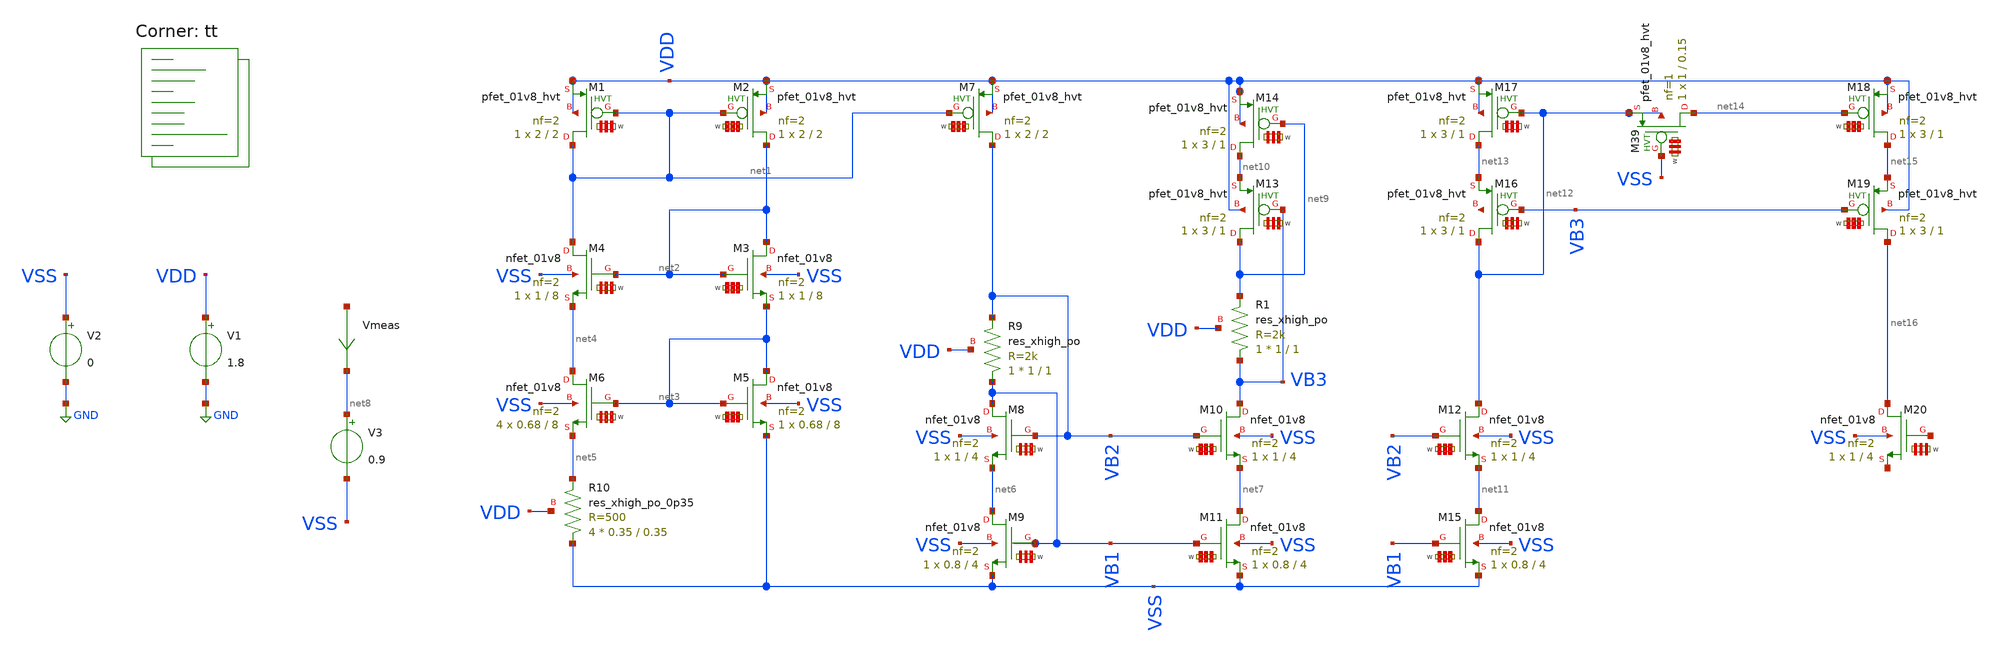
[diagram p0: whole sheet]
** sch_path: my_ip/sky130A/VFCOA_v1/testbench.sch
**.subckt testbench
V1 VDD GND 1.8
V2 VSS GND 0
V3 net8 VSS 0.9
XM5 net3 net3 VSS VSS sky130_fd_pr__nfet_01v8 L=8 W='0.68 * 2 ' nf=2 ad='int((2 + 1)/2) * 0.68 / 2 * 0.29'
+ as='int((2 + 2)/2) * 0.68 / 2 * 0.29' pd='2*int((2 + 1)/2) * (0.68 / 2 + 0.29)' ps='2*int((2 + 2)/2) * (0.68 / 2 + 0.29)'
+ nrd='0.29 / 0.68 ' nrs='0.29 / 0.68 ' sa=0 sb=0 sd=0 mult=1 m=1
XM6 net4 net3 net5 VSS sky130_fd_pr__nfet_01v8 L=8 W='0.68 * 2 ' nf=2 ad='int((2 + 1)/2) * 0.68 / 2 * 0.29'
+ as='int((2 + 2)/2) * 0.68 / 2 * 0.29' pd='2*int((2 + 1)/2) * (0.68 / 2 + 0.29)' ps='2*int((2 + 2)/2) * (0.68 / 2 + 0.29)'
+ nrd='0.29 / 0.68 ' nrs='0.29 / 0.68 ' sa=0 sb=0 sd=0 mult=4 m=4
XM2 net2 net1 VDD VDD sky130_fd_pr__pfet_01v8_hvt L=2 W='2 * 2 ' nf=2 ad='int((2 + 1)/2) * 2 / 2 * 0.29'
+ as='int((2 + 2)/2) * 2 / 2 * 0.29' pd='2*int((2 + 1)/2) * (2 / 2 + 0.29)' ps='2*int((2 + 2)/2) * (2 / 2 + 0.29)'
+ nrd='0.29 / 2 ' nrs='0.29 / 2 ' sa=0 sb=0 sd=0 mult=1 m=1
XM1 net1 net1 VDD VDD sky130_fd_pr__pfet_01v8_hvt L=2 W='2 * 2 ' nf=2 ad='int((2 + 1)/2) * 2 / 2 * 0.29'
+ as='int((2 + 2)/2) * 2 / 2 * 0.29' pd='2*int((2 + 1)/2) * (2 / 2 + 0.29)' ps='2*int((2 + 2)/2) * (2 / 2 + 0.29)'
+ nrd='0.29 / 2 ' nrs='0.29 / 2 ' sa=0 sb=0 sd=0 mult=1 m=1
XR10 VSS net5 VDD sky130_fd_pr__res_xhigh_po_0p35 L=0.35 mult=4 m=4
XM4 net1 net2 net4 VSS sky130_fd_pr__nfet_01v8 L=8 W='1 * 2 ' nf=2 ad='int((2 + 1)/2) * 1 / 2 * 0.29'
+ as='int((2 + 2)/2) * 1 / 2 * 0.29' pd='2*int((2 + 1)/2) * (1 / 2 + 0.29)' ps='2*int((2 + 2)/2) * (1 / 2 + 0.29)'
+ nrd='0.29 / 1 ' nrs='0.29 / 1 ' sa=0 sb=0 sd=0 mult=1 m=1
XM3 net2 net2 net3 VSS sky130_fd_pr__nfet_01v8 L=8 W='1 * 2 ' nf=2 ad='int((2 + 1)/2) * 1 / 2 * 0.29'
+ as='int((2 + 2)/2) * 1 / 2 * 0.29' pd='2*int((2 + 1)/2) * (1 / 2 + 0.29)' ps='2*int((2 + 2)/2) * (1 / 2 + 0.29)'
+ nrd='0.29 / 1 ' nrs='0.29 / 1 ' sa=0 sb=0 sd=0 mult=1 m=1
XM7 VB2 net1 VDD VDD sky130_fd_pr__pfet_01v8_hvt L=2 W='2 * 2 ' nf=2 ad='int((2 + 1)/2) * 2 / 2 * 0.29'
+ as='int((2 + 2)/2) * 2 / 2 * 0.29' pd='2*int((2 + 1)/2) * (2 / 2 + 0.29)' ps='2*int((2 + 2)/2) * (2 / 2 + 0.29)'
+ nrd='0.29 / 2 ' nrs='0.29 / 2 ' sa=0 sb=0 sd=0 mult=1 m=1
Vmeas net17 net8 0
.save i(vmeas)
XM10 VB3 VB2 net7 VSS sky130_fd_pr__nfet_01v8 L=4 W='1 * 2 ' nf=2 ad='int((2 + 1)/2) * 1 / 2 * 0.29'
+ as='int((2 + 2)/2) * 1 / 2 * 0.29' pd='2*int((2 + 1)/2) * (1 / 2 + 0.29)' ps='2*int((2 + 2)/2) * (1 / 2 + 0.29)'
+ nrd='0.29 / 1 ' nrs='0.29 / 1 ' sa=0 sb=0 sd=0 mult=1 m=1
XR9 VB1 VB2 VDD sky130_fd_pr__res_xhigh_po W=1 L=1 mult=1 m=1
XM11 net7 VB1 VSS VSS sky130_fd_pr__nfet_01v8 L=4 W='0.8 * 2 ' nf=2 ad='int((2 + 1)/2) * 0.8 / 2 * 0.29'
+ as='int((2 + 2)/2) * 0.8 / 2 * 0.29' pd='2*int((2 + 1)/2) * (0.8 / 2 + 0.29)' ps='2*int((2 + 2)/2) * (0.8 / 2 + 0.29)'
+ nrd='0.29 / 0.8 ' nrs='0.29 / 0.8 ' sa=0 sb=0 sd=0 mult=1 m=1
XM8 VB1 VB2 net6 VSS sky130_fd_pr__nfet_01v8 L=4 W='1 * 2 ' nf=2 ad='int((2 + 1)/2) * 1 / 2 * 0.29' as='int((2 + 2)/2) * 1 / 2 * 0.29'
+ pd='2*int((2 + 1)/2) * (1 / 2 + 0.29)' ps='2*int((2 + 2)/2) * (1 / 2 + 0.29)' nrd='0.29 / 1 ' nrs='0.29 / 1 '
+ sa=0 sb=0 sd=0 mult=1 m=1
XM9 net6 VB1 VSS VSS sky130_fd_pr__nfet_01v8 L=4 W='0.8 * 2 ' nf=2 ad='int((2 + 1)/2) * 0.8 / 2 * 0.29'
+ as='int((2 + 2)/2) * 0.8 / 2 * 0.29' pd='2*int((2 + 1)/2) * (0.8 / 2 + 0.29)' ps='2*int((2 + 2)/2) * (0.8 / 2 + 0.29)'
+ nrd='0.29 / 0.8 ' nrs='0.29 / 0.8 ' sa=0 sb=0 sd=0 mult=1 m=1
XR1 VB3 net9 VDD sky130_fd_pr__res_xhigh_po W=1 L=1 mult=1 m=1
XM13 net9 VB3 net10 VDD sky130_fd_pr__pfet_01v8_hvt L=1 W='3 * 2 ' nf=2 ad='int((2 + 1)/2) * 3 / 2 * 0.29'
+ as='int((2 + 2)/2) * 3 / 2 * 0.29' pd='2*int((2 + 1)/2) * (3 / 2 + 0.29)' ps='2*int((2 + 2)/2) * (3 / 2 + 0.29)'
+ nrd='0.29 / 3 ' nrs='0.29 / 3 ' sa=0 sb=0 sd=0 mult=1 m=1
XM14 net10 net9 VDD VDD sky130_fd_pr__pfet_01v8_hvt L=1 W='3 * 2 ' nf=2 ad='int((2 + 1)/2) * 3 / 2 * 0.29'
+ as='int((2 + 2)/2) * 3 / 2 * 0.29' pd='2*int((2 + 1)/2) * (3 / 2 + 0.29)' ps='2*int((2 + 2)/2) * (3 / 2 + 0.29)'
+ nrd='0.29 / 3 ' nrs='0.29 / 3 ' sa=0 sb=0 sd=0 mult=1 m=1
XM12 net12 VB2 net11 VSS sky130_fd_pr__nfet_01v8 L=4 W='1 * 2 ' nf=2 ad='int((2 + 1)/2) * 1 / 2 * 0.29'
+ as='int((2 + 2)/2) * 1 / 2 * 0.29' pd='2*int((2 + 1)/2) * (1 / 2 + 0.29)' ps='2*int((2 + 2)/2) * (1 / 2 + 0.29)'
+ nrd='0.29 / 1 ' nrs='0.29 / 1 ' sa=0 sb=0 sd=0 mult=1 m=1
XM15 net11 VB1 VSS VSS sky130_fd_pr__nfet_01v8 L=4 W='0.8 * 2 ' nf=2 ad='int((2 + 1)/2) * 0.8 / 2 * 0.29'
+ as='int((2 + 2)/2) * 0.8 / 2 * 0.29' pd='2*int((2 + 1)/2) * (0.8 / 2 + 0.29)' ps='2*int((2 + 2)/2) * (0.8 / 2 + 0.29)'
+ nrd='0.29 / 0.8 ' nrs='0.29 / 0.8 ' sa=0 sb=0 sd=0 mult=1 m=1
XM16 net12 VB3 net13 net18 sky130_fd_pr__pfet_01v8_hvt L=1 W='3 * 2 ' nf=2 ad='int((2 + 1)/2) * 3 / 2 * 0.29'
+ as='int((2 + 2)/2) * 3 / 2 * 0.29' pd='2*int((2 + 1)/2) * (3 / 2 + 0.29)' ps='2*int((2 + 2)/2) * (3 / 2 + 0.29)'
+ nrd='0.29 / 3 ' nrs='0.29 / 3 ' sa=0 sb=0 sd=0 mult=1 m=1
XM17 net13 net12 VDD VDD sky130_fd_pr__pfet_01v8_hvt L=1 W='3 * 2 ' nf=2 ad='int((2 + 1)/2) * 3 / 2 * 0.29'
+ as='int((2 + 2)/2) * 3 / 2 * 0.29' pd='2*int((2 + 1)/2) * (3 / 2 + 0.29)' ps='2*int((2 + 2)/2) * (3 / 2 + 0.29)'
+ nrd='0.29 / 3 ' nrs='0.29 / 3 ' sa=0 sb=0 sd=0 mult=1 m=1
XM39 net14 VSS net12 net12 sky130_fd_pr__pfet_01v8_hvt L=0.15 W='1 * 1 ' nf=1 ad='int((1 + 1)/2) * 1 / 1 * 0.29'
+ as='int((1 + 2)/2) * 1 / 1 * 0.29' pd='2*int((1 + 1)/2) * (1 / 1 + 0.29)' ps='2*int((1 + 2)/2) * (1 / 1 + 0.29)'
+ nrd='0.29 / 1 ' nrs='0.29 / 1 ' sa=0 sb=0 sd=0 mult=1 m=1
XM18 net15 net14 VDD VDD sky130_fd_pr__pfet_01v8_hvt L=1 W='3 * 2 ' nf=2 ad='int((2 + 1)/2) * 3 / 2 * 0.29'
+ as='int((2 + 2)/2) * 3 / 2 * 0.29' pd='2*int((2 + 1)/2) * (3 / 2 + 0.29)' ps='2*int((2 + 2)/2) * (3 / 2 + 0.29)'
+ nrd='0.29 / 3 ' nrs='0.29 / 3 ' sa=0 sb=0 sd=0 mult=1 m=1
XM19 net16 VB3 net15 VDD sky130_fd_pr__pfet_01v8_hvt L=1 W='3 * 2 ' nf=2 ad='int((2 + 1)/2) * 3 / 2 * 0.29'
+ as='int((2 + 2)/2) * 3 / 2 * 0.29' pd='2*int((2 + 1)/2) * (3 / 2 + 0.29)' ps='2*int((2 + 2)/2) * (3 / 2 + 0.29)'
+ nrd='0.29 / 3 ' nrs='0.29 / 3 ' sa=0 sb=0 sd=0 mult=1 m=1
XM20 net16 net19 net20 VSS sky130_fd_pr__nfet_01v8 L=4 W='1 * 2 ' nf=2 ad='int((2 + 1)/2) * 1 / 2 * 0.29'
+ as='int((2 + 2)/2) * 1 / 2 * 0.29' pd='2*int((2 + 1)/2) * (1 / 2 + 0.29)' ps='2*int((2 + 2)/2) * (1 / 2 + 0.29)'
+ nrd='0.29 / 1 ' nrs='0.29 / 1 ' sa=0 sb=0 sd=0 mult=1 m=1
**** begin user architecture code
.lib $::SKYWATER_MODELS/sky130.lib.spice tt

**************************************************************
**************************************************************
**************************************************************
**************************************************************
**************************************************************
*LIBs*********************************************************
**************************************************************
**************************************************************
**************************************************************
**************************************************************
**************************************************************
*.lib $::SKYWATER_MODELS/sky130.lib.spice tt
* chose the corners in the corner file
* tt_mm for mismatch
* ss ff sf fs standart corners
* ll hh lh hl capacitor and resistors corners
* mc for total process variation including corners
**************************************************************
**************************************************************
**************************************************************
**************************************************************
**************************************************************
*Corners/montecarlo options***********************************
**************************************************************
**************************************************************
**************************************************************
**************************************************************
**************************************************************
.TEMP 27
**************************************************************
**************************************************************
**************************************************************
**************************************************************
*SIMULATION and Plots*****************************************
**************************************************************
**************************************************************
**************************************************************
**************************************************************
.control
save all
dc V3 0 1.8 0.001
*dc simulation
plot i(Vmeas)
.endc

**** end user architecture code
**.ends
.GLOBAL GND
.end
